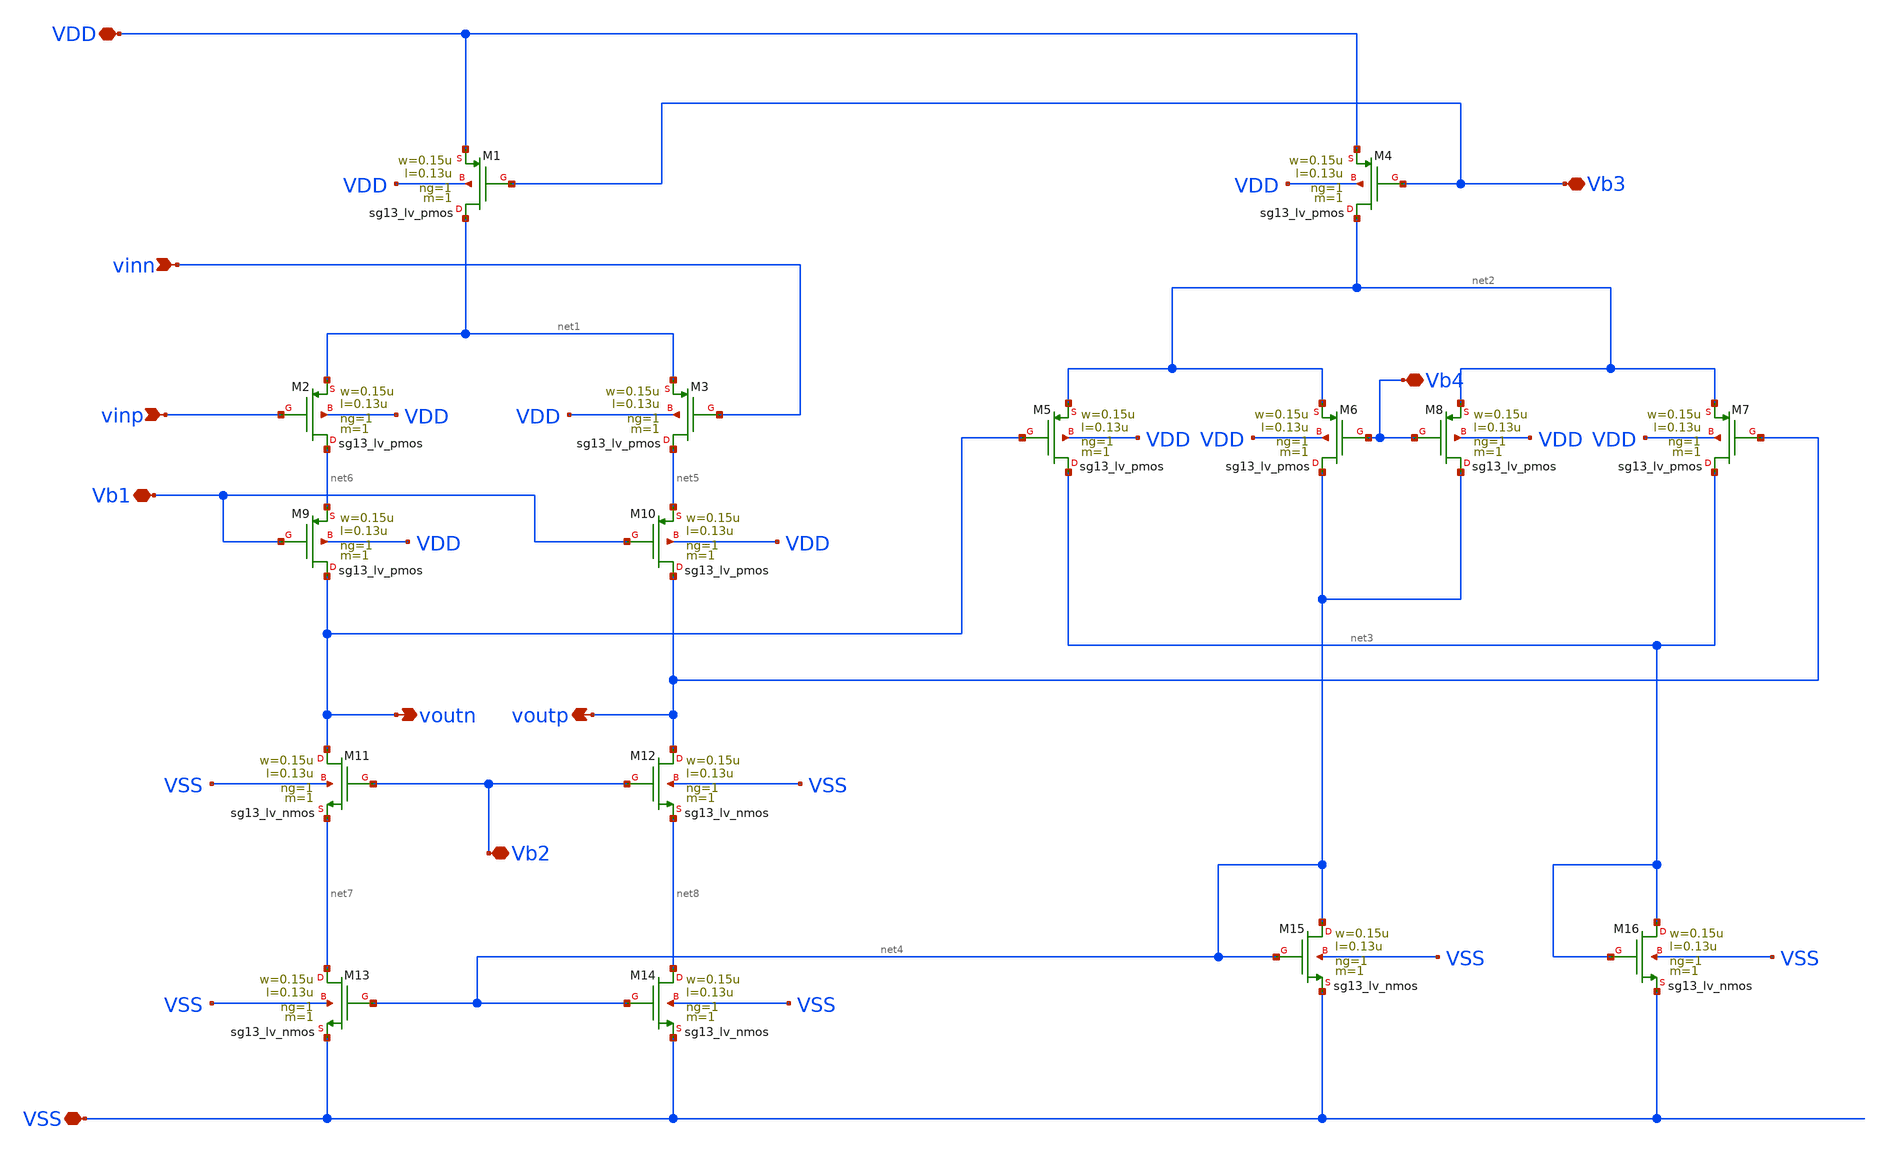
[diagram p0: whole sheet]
** sch_path: analog-db/circuits/amp_027_fan_rrl_ota/pdk/ihp-sg13g2/schematic/integrator-switchcap-opamp.sch
* Copyright 2026 MacAnalog Research Group
**.subckt integrator-switchcap-opamp VDD vinp vinn Vb3 Vb1 VSS Vb2 voutn voutp Vb4
*.iopin VDD
*.ipin vinp
*.ipin vinn
*.iopin Vb3
*.iopin Vb1
*.iopin VSS
*.iopin Vb2
*.opin voutn
*.opin voutp
*.iopin Vb4
XM1 net1 Vb3 VDD VDD sg13_lv_pmos w=0.15u l=0.13u ng=1 m=1 mm_ok=1
XM2 net6 vinp net1 VDD sg13_lv_pmos w=0.15u l=0.13u ng=1 m=1 mm_ok=1
XM3 net5 vinn net1 VDD sg13_lv_pmos w=0.15u l=0.13u ng=1 m=1 mm_ok=1
XM4 net2 Vb3 VDD VDD sg13_lv_pmos w=0.15u l=0.13u ng=1 m=1 mm_ok=1
XM5 net3 voutn net2 VDD sg13_lv_pmos w=0.15u l=0.13u ng=1 m=1 mm_ok=1
XM6 net4 Vb4 net2 VDD sg13_lv_pmos w=0.15u l=0.13u ng=1 m=1 mm_ok=1
XM7 net3 voutp net2 VDD sg13_lv_pmos w=0.15u l=0.13u ng=1 m=1 mm_ok=1
XM8 net4 Vb4 net2 VDD sg13_lv_pmos w=0.15u l=0.13u ng=1 m=1 mm_ok=1
XM9 voutn Vb1 net6 VDD sg13_lv_pmos w=0.15u l=0.13u ng=1 m=1 mm_ok=1
XM10 voutp Vb1 net5 VDD sg13_lv_pmos w=0.15u l=0.13u ng=1 m=1 mm_ok=1
XM11 voutn Vb2 net7 VSS sg13_lv_nmos w=0.15u l=0.13u ng=1 m=1 mm_ok=1
XM12 voutp Vb2 net8 VSS sg13_lv_nmos w=0.15u l=0.13u ng=1 m=1 mm_ok=1
XM13 net7 net4 VSS VSS sg13_lv_nmos w=0.15u l=0.13u ng=1 m=1 mm_ok=1
XM14 net8 net4 VSS VSS sg13_lv_nmos w=0.15u l=0.13u ng=1 m=1 mm_ok=1
XM15 net4 net4 VSS VSS sg13_lv_nmos w=0.15u l=0.13u ng=1 m=1 mm_ok=1
XM16 net3 net3 VSS VSS sg13_lv_nmos w=0.15u l=0.13u ng=1 m=1 mm_ok=1
**.ends
.end
